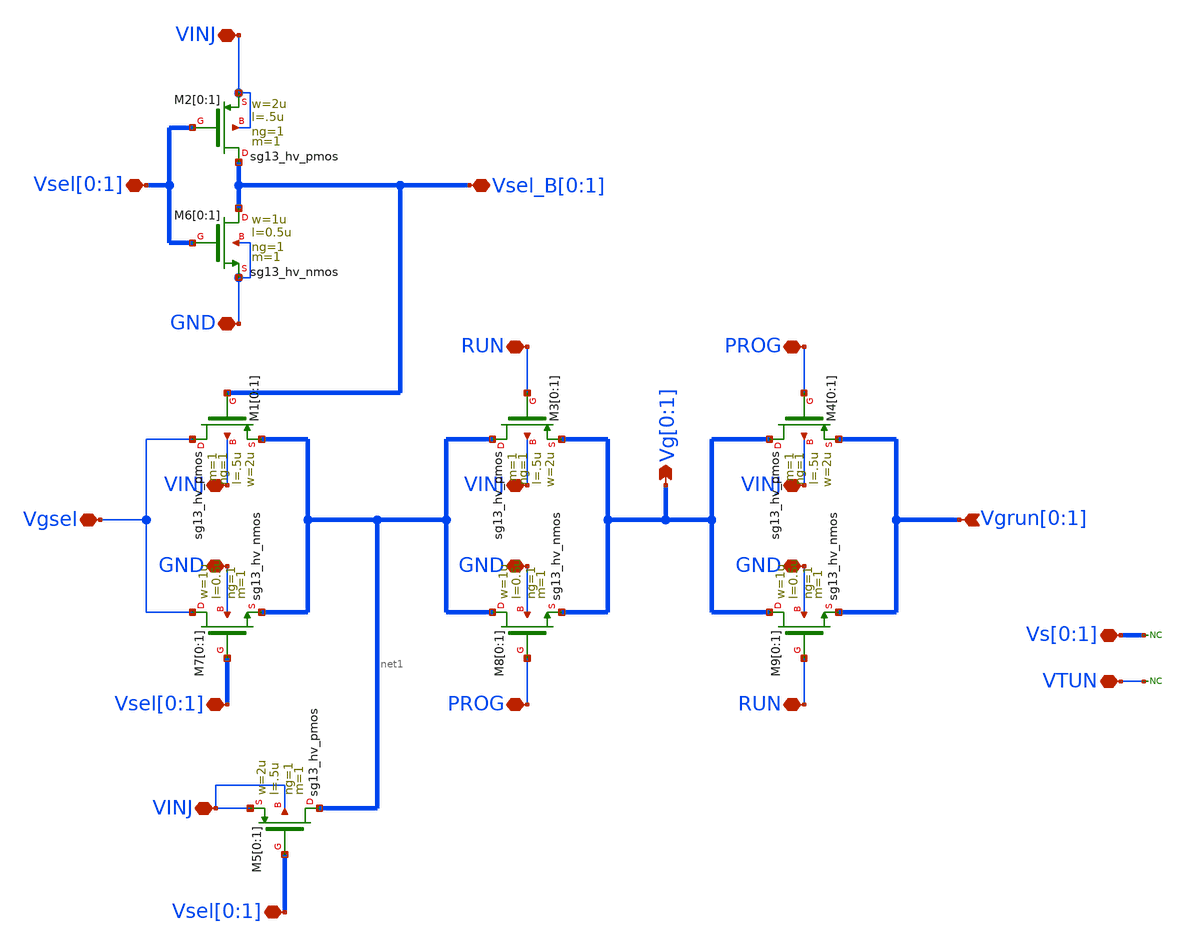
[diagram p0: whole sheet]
** sch_path: ihp130_cells/IndirectVMM_GSwcs_1x2/IndirectVMM_GSwcs_1x2.sch
**.subckt IndirectVMM_GSwcs_1x2 VINJ GND Vgrun[0],Vgrun[1] Vg[0],Vg[1] Vsel[0],Vsel[1]
*+ Vsel_B[0],Vsel_B[1] Vgsel Vsel[0],Vsel[1] RUN PROG VINJ VINJ GND Vsel[0],Vsel[1] VINJ GND RUN PROG VINJ GND Vs[0],Vs[1]
*+ VTUN
*.iopin VINJ
*.iopin GND
*.ipin Vgrun[0],Vgrun[1]
*.opin Vg[0],Vg[1]
*.iopin Vsel[0],Vsel[1]
*.iopin Vsel_B[0],Vsel_B[1]
*.iopin Vgsel
*.iopin Vsel[0],Vsel[1]
*.iopin RUN
*.iopin PROG
*.iopin VINJ
*.iopin VINJ
*.iopin GND
*.iopin Vsel[0],Vsel[1]
*.iopin VINJ
*.iopin GND
*.iopin RUN
*.iopin PROG
*.iopin VINJ
*.iopin GND
*.iopin Vs[0],Vs[1]
*.iopin VTUN
* noconn Vs[0:1]
* noconn VTUN
XM2[0] Vsel_B[0] Vsel[0] VINJ VINJ sg13_hv_pmos w=2u l=.5u ng=1 m=1 mm_ok=1
XM2[1] Vsel_B[1] Vsel[1] VINJ VINJ sg13_hv_pmos w=2u l=.5u ng=1 m=1 mm_ok=1
XM1[0] Vgsel Vsel_B[0] net1[1] VINJ sg13_hv_pmos w=2u l=.5u ng=1 m=1 mm_ok=1
XM1[1] Vgsel Vsel_B[1] net1[0] VINJ sg13_hv_pmos w=2u l=.5u ng=1 m=1 mm_ok=1
XM5[0] net1[1] Vsel[0] VINJ VINJ sg13_hv_pmos w=2u l=.5u ng=1 m=1 mm_ok=1
XM5[1] net1[0] Vsel[1] VINJ VINJ sg13_hv_pmos w=2u l=.5u ng=1 m=1 mm_ok=1
XM3[0] net1[1] RUN Vg[0] VINJ sg13_hv_pmos w=2u l=.5u ng=1 m=1 mm_ok=1
XM3[1] net1[0] RUN Vg[1] VINJ sg13_hv_pmos w=2u l=.5u ng=1 m=1 mm_ok=1
XM4[0] Vg[0] PROG Vgrun[0] VINJ sg13_hv_pmos w=2u l=.5u ng=1 m=1 mm_ok=1
XM4[1] Vg[1] PROG Vgrun[1] VINJ sg13_hv_pmos w=2u l=.5u ng=1 m=1 mm_ok=1
XM6[0] Vsel_B[0] Vsel[0] GND GND sg13_hv_nmos w=1u l=0.5u ng=1 m=1 mm_ok=1
XM6[1] Vsel_B[1] Vsel[1] GND GND sg13_hv_nmos w=1u l=0.5u ng=1 m=1 mm_ok=1
XM7[0] Vgsel Vsel[0] net1[1] GND sg13_hv_nmos w=1u l=0.5u ng=1 m=1 mm_ok=1
XM7[1] Vgsel Vsel[1] net1[0] GND sg13_hv_nmos w=1u l=0.5u ng=1 m=1 mm_ok=1
XM8[0] net1[1] PROG Vg[0] GND sg13_hv_nmos w=1u l=0.5u ng=1 m=1 mm_ok=1
XM8[1] net1[0] PROG Vg[1] GND sg13_hv_nmos w=1u l=0.5u ng=1 m=1 mm_ok=1
XM9[0] Vg[0] RUN Vgrun[0] GND sg13_hv_nmos w=1u l=0.5u ng=1 m=1 mm_ok=1
XM9[1] Vg[1] RUN Vgrun[1] GND sg13_hv_nmos w=1u l=0.5u ng=1 m=1 mm_ok=1
**.ends
.end
